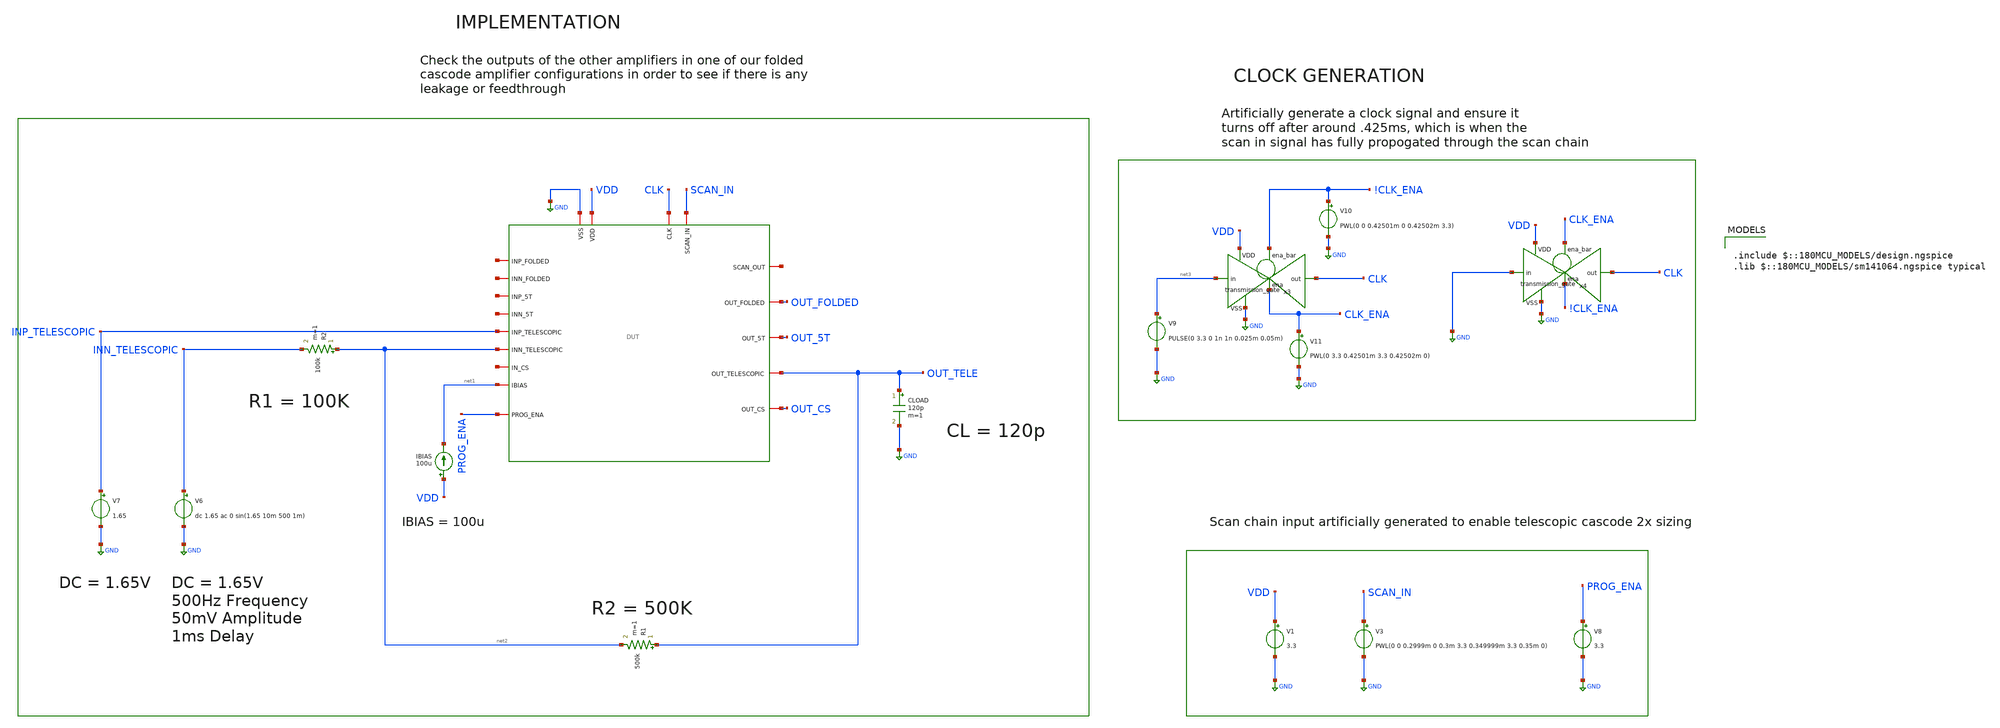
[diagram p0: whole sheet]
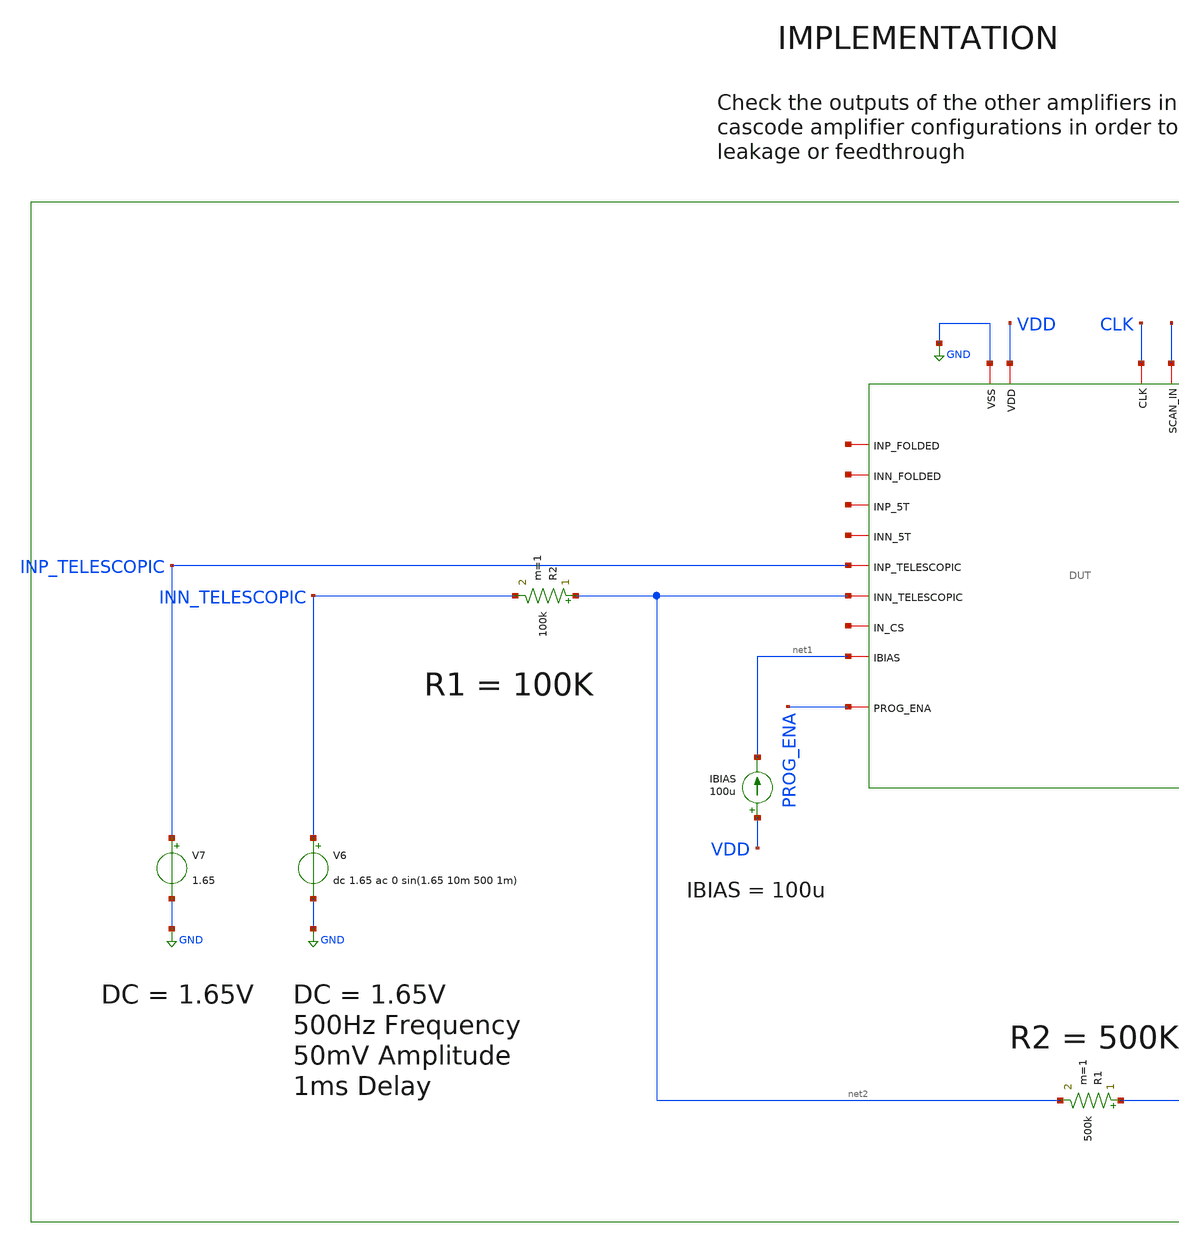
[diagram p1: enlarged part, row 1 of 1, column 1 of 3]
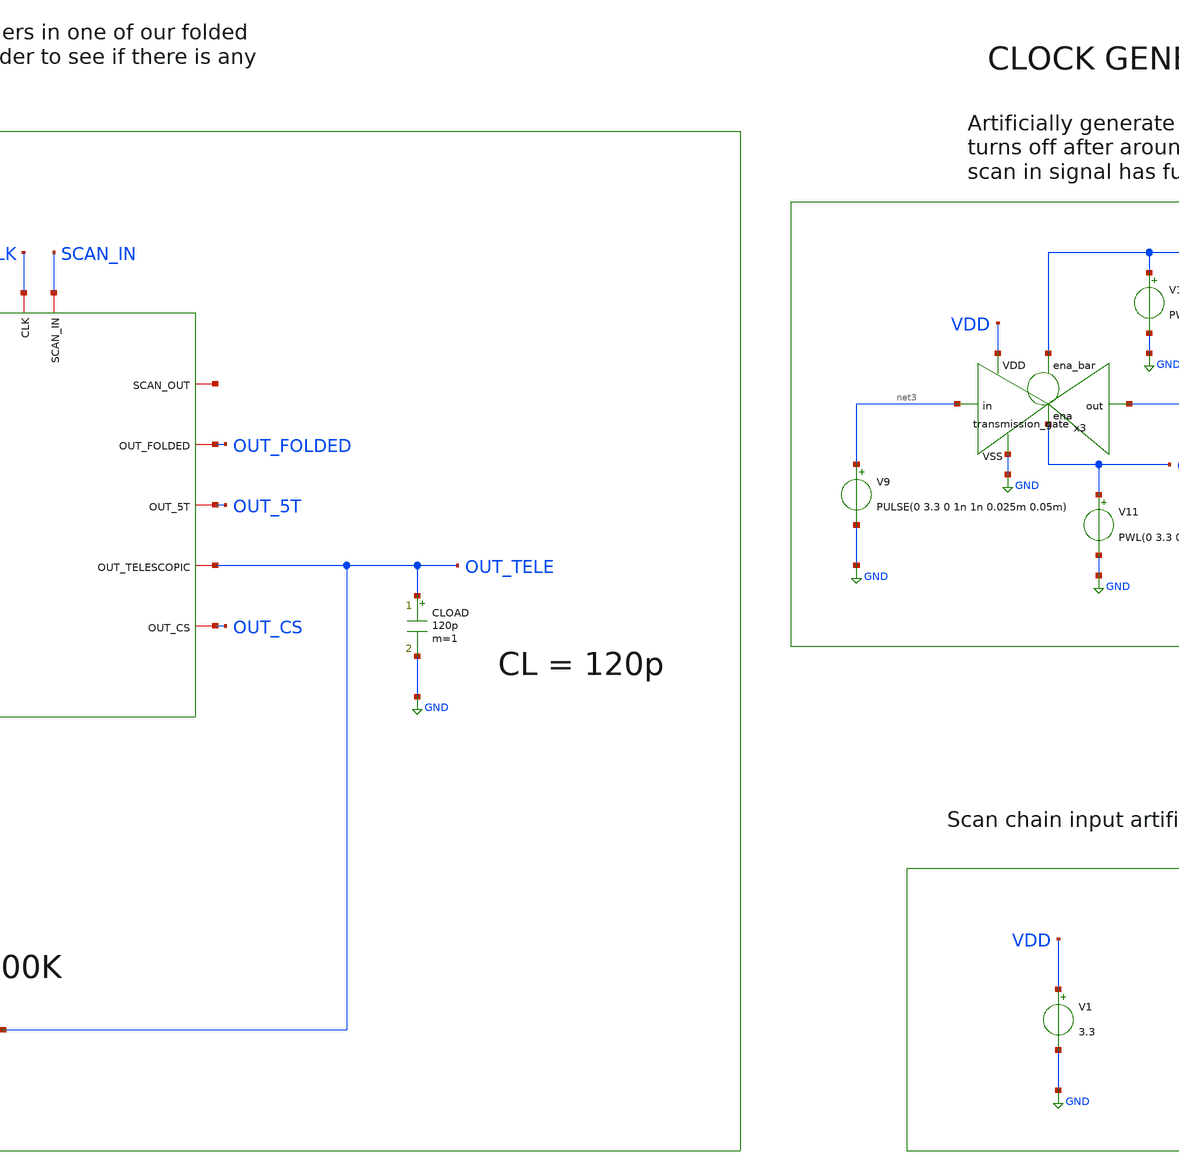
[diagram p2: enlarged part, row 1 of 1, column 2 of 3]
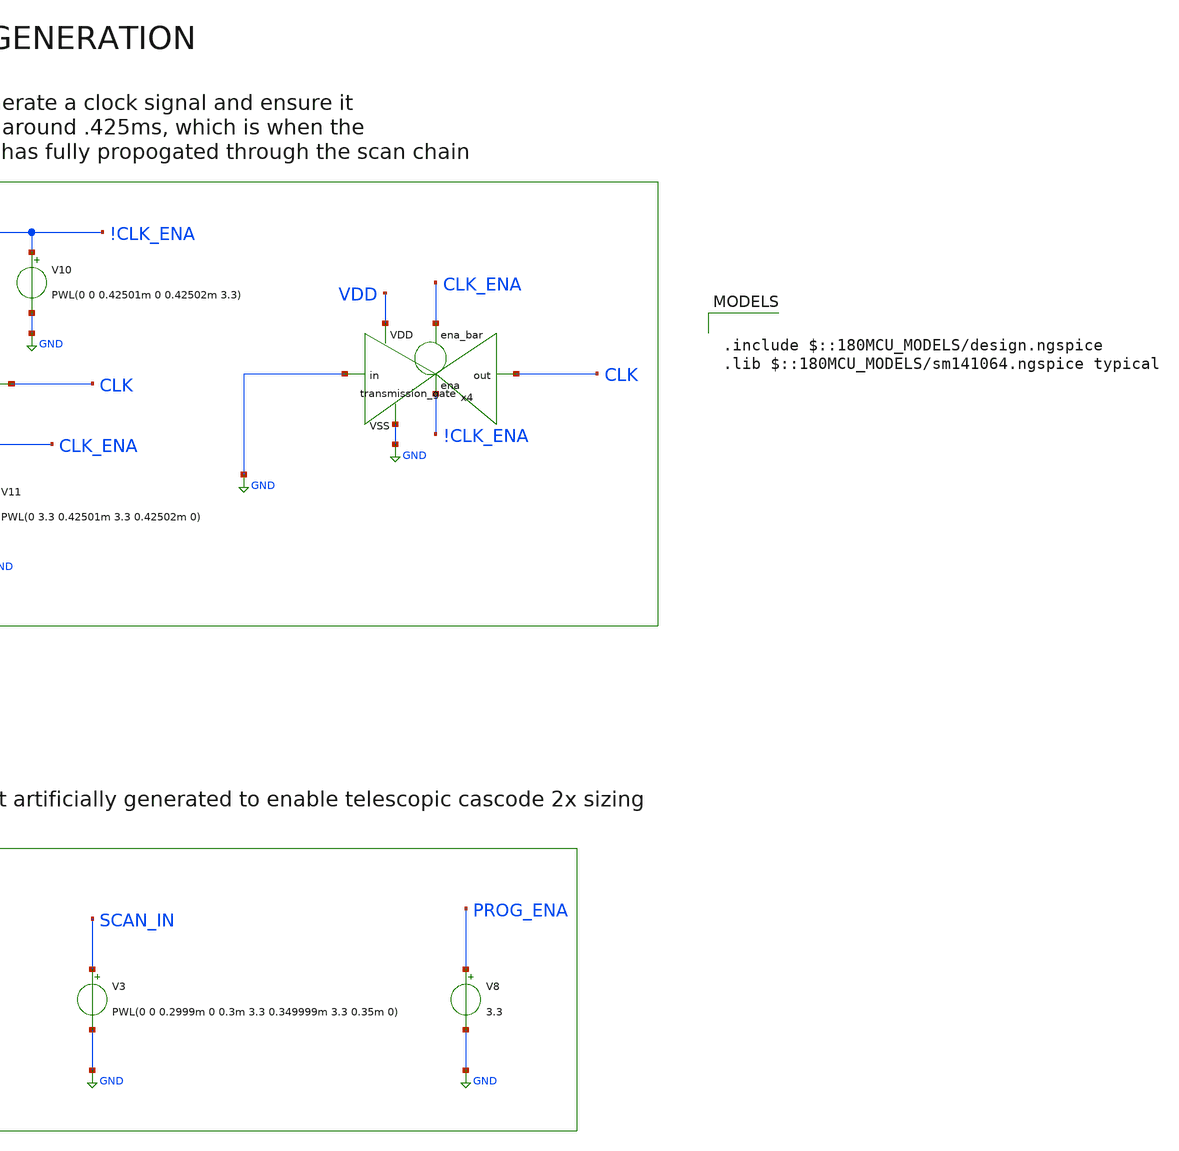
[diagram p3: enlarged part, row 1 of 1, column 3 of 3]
** sch_path: designs/libs/verification/ota_telescopic/2x/iso.sch
**.subckt iso
V1 VDD GND 3.3
IBIAS VDD net1 100u
V7 INP_TELESCOPIC GND 1.65
CLOAD OUT_TELE GND 120p m=1
R2 net2 INN_TELESCOPIC 100k m=1
V6 INN_TELESCOPIC GND dc 1.65 ac 0 sin(1.65 10m 500 1m)
R1 OUT_TELE net2 500k m=1
x1 CLK net4 SCAN_IN GND VDD OUT_FOLDED net5 OUT_5T net1 net6 net7 net8 INP_TELESCOPIC OUT_TELE
+ OUT_CS net9 net2 PROG_ENA DUT
V8 PROG_ENA GND 3.3
V9 net3 GND PULSE(0 3.3 0 1n 1n 0.025m 0.05m)
x3 !CLK_ENA VDD CLK net3 GND CLK_ENA transmission_gate
V10 !CLK_ENA GND PWL(0 0 0.42501m 0 0.42502m 3.3)
V11 CLK_ENA GND PWL(0 3.3 0.42501m 3.3 0.42502m 0)
x4 CLK_ENA VDD CLK GND GND !CLK_ENA transmission_gate
V3 SCAN_IN GND PWL(0 0 0.2999m 0 0.3m 3.3 0.349999m 3.3 0.35m 0)
**** begin user architecture code

.include $::180MCU_MODELS/design.ngspice
.lib $::180MCU_MODELS/sm141064.ngspice typical



.control
tran 1u 5m

plot v(out_folded) v(out_5t) v(out_tele) v(out_cs)

meas tran folded_pp pp v(out_folded) from=2m to=5m
meas tran five_t_pp pp v(out_5t) from=2m to=5m
meas tran tele_pp pp v(out_tele) from=2m to=5m
meas tran cs_pp pp v(out_cs) from=2m to=5m

print folded_pp five_t_pp tele_pp cs_pp

let iso_5t = 20 * log(five_t_pp / tele_pp) / log(10)
let iso_folded = 20 * log(folded_pp / tele_pp) / log(10)
let iso_cs = 20 * log(cs_pp / tele_pp) / log(10)

print iso_5t iso_folded iso_cs
.endc


**** end user architecture code
**.ends
.GLOBAL GND
.end
